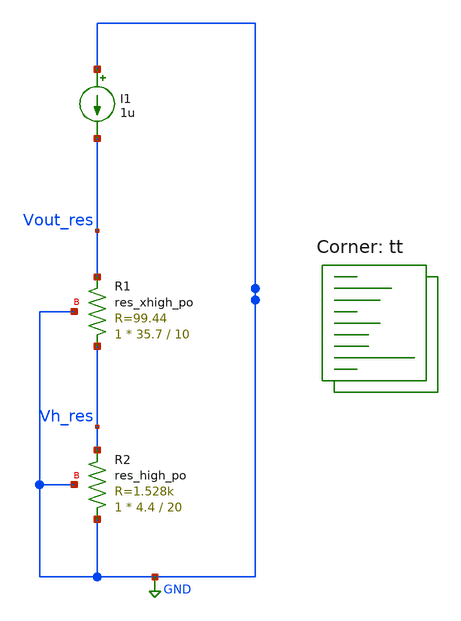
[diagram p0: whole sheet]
** sch_path: xschem/misc/testing/res_slope_cancel.sch
**.subckt res_slope_cancel
I1 GND Vout_res 1u
XR2 GND Vh_res GND sky130_fd_pr__res_high_po W=4.4 L=20 mult=1 m=1
XR1 Vh_res Vout_res GND sky130_fd_pr__res_xhigh_po W=35.7 L=10 mult=1 m=1
**** begin user architecture code
.lib $::SKYWATER_MODELS/sky130.lib.spice tt


.param temp=27

.dc temp -40 125 1


.save all
.control
run
plot Vout_res
plot deriv(Vout_res)
.endc



**** end user architecture code
**.ends
.GLOBAL GND
.end
